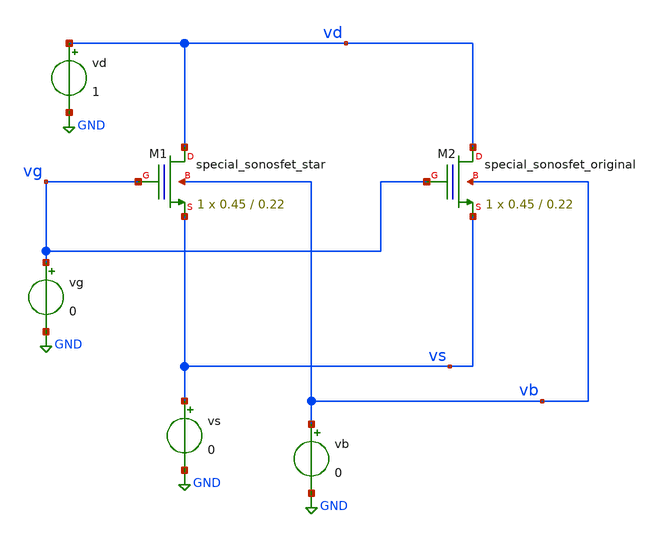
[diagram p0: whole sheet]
** sch_path: sonos/sonos_curves_simple.sch
**.subckt sonos_curves_simple
XM1 vd vg vs vb sky130_fd_bs_flash__special_sonosfet_star L=0.22 W=0.45 nf=1 ad='1 * W * 0.29' as='1 * W * 0.29'
+ pd='2 * (W + 0.29)' ps='2 * (W + 0.29)' nrd='0.29 / W' nrs='0.29 / W' sa=0 sb=0 sd=0 mult=1 m=1
XM2 vd vg vs vb sky130_fd_bs_flash__special_sonosfet_original L=0.22 W=0.45 nf=1 ad='1 * W * 0.29' as='1 * W * 0.29'
+ pd='2 * (W + 0.29)' ps='2 * (W + 0.29)' nrd='0.29 / W' nrs='0.29 / W' sa=0 sb=0 sd=0 mult=1 m=1
vg vg GND 0
vd vd GND 1
vs vs GND 0
vb vb GND 0
**** begin user architecture code

** opencircuitdesign pdks install
.lib $::SKYWATER_MODELS/sky130.lib.spice tt
.include $::SKYWATER_MODELS/sonos_see_e/begin_of_life.spice
.include $::SKYWATER_MODELS/sonos_see_e/begin_of_life.pm3.spice
.include $::SKYWATER_MODELS/sonos_see_p/begin_of_life.spice
.include $::SKYWATER_MODELS/sonos_see_p/begin_of_life.pm3.spice



.option savecurrents
*.option abstol=1e-10 reltol=1e-2 chgtol=1e-12
*.ic v(bootp)=0 v(bootn)=0 v(inp)=0 v(inn)=0 v(inf)=0 v(inb)=0
*.ic v(net3)=0 v(net4)=0
.control
  unset appendwrite
  save all

  dc vd 0 1 0.1 vg 0 2 0.5
  remzerovec
  write test_sonos_curves_simple.raw
.endc


**** end user architecture code
**.ends
.GLOBAL GND
.end
